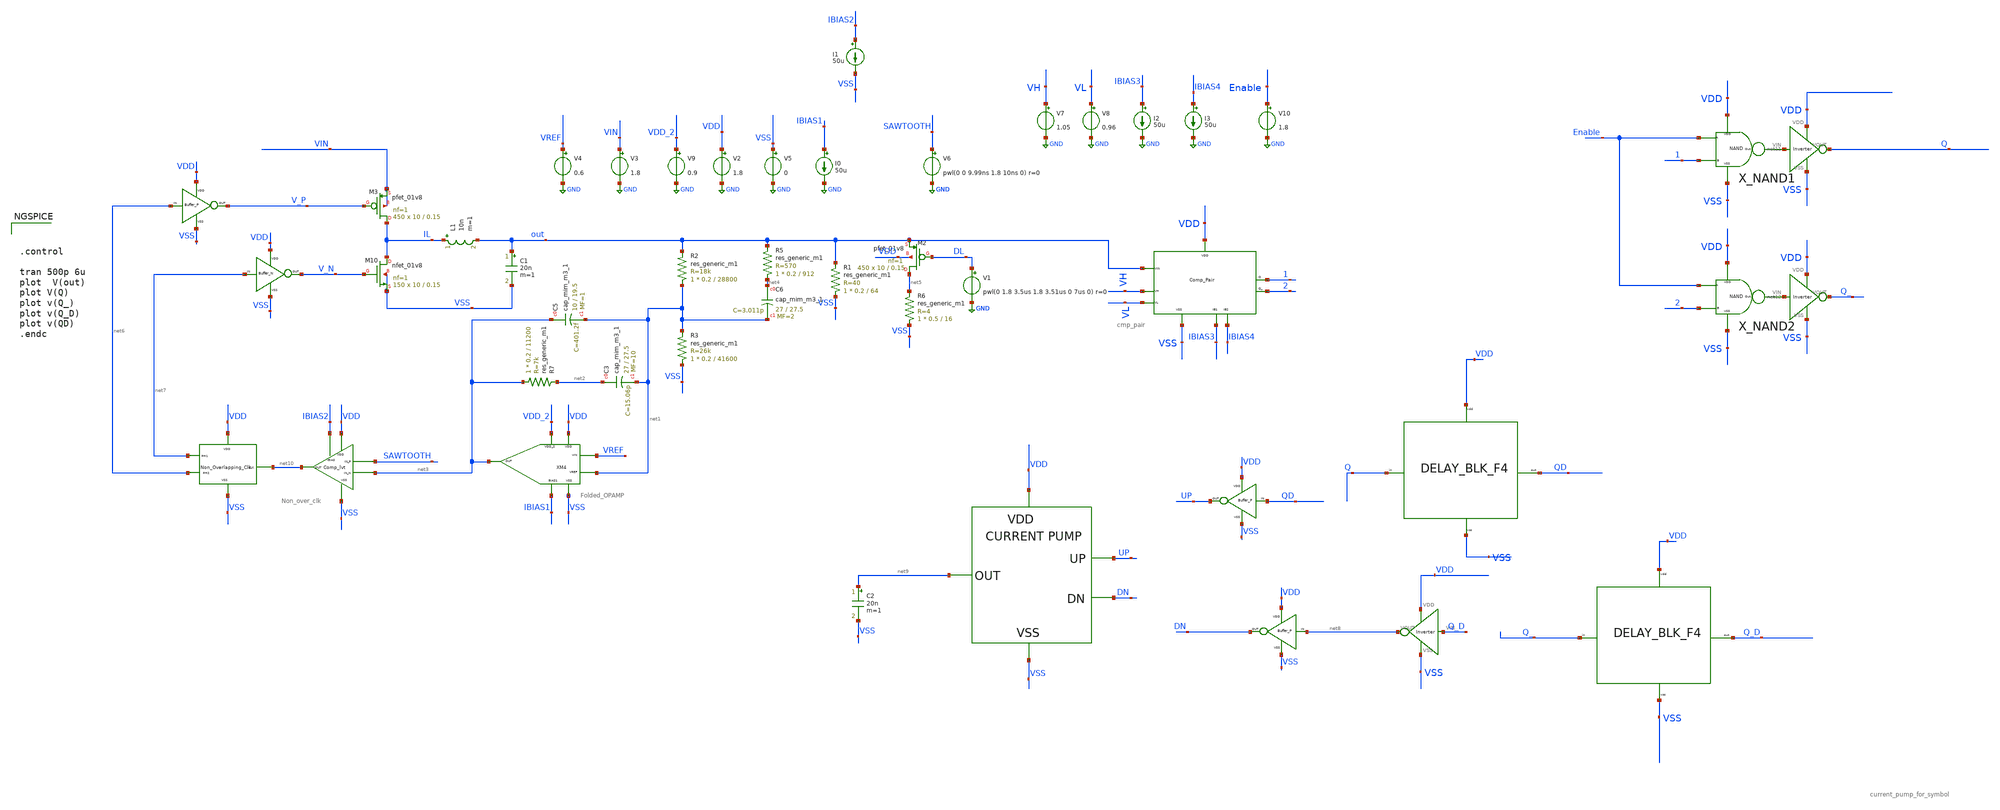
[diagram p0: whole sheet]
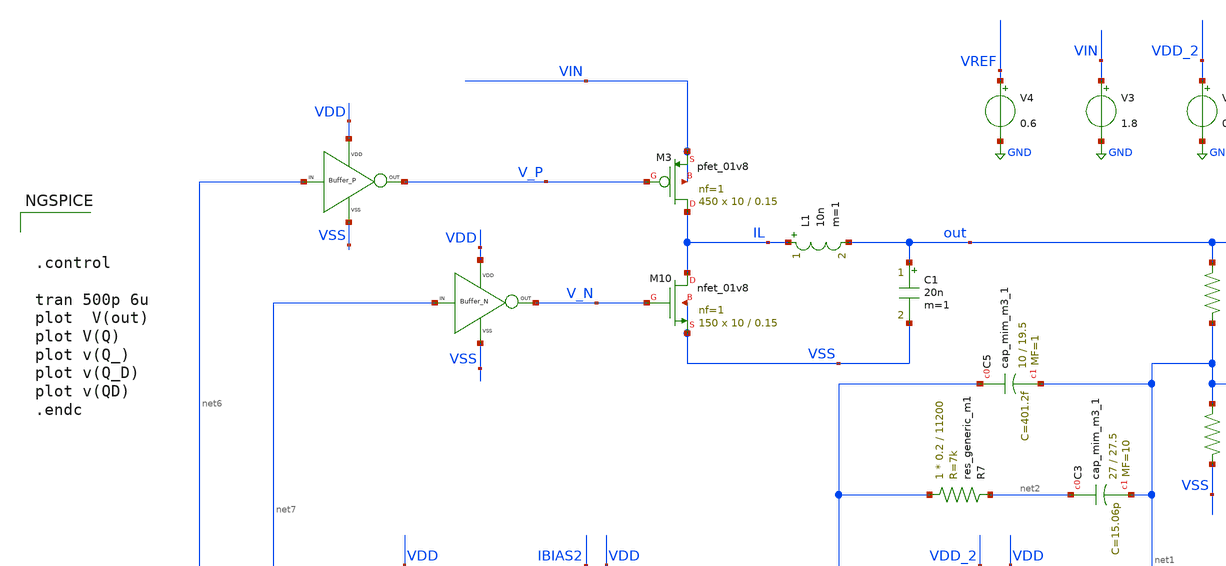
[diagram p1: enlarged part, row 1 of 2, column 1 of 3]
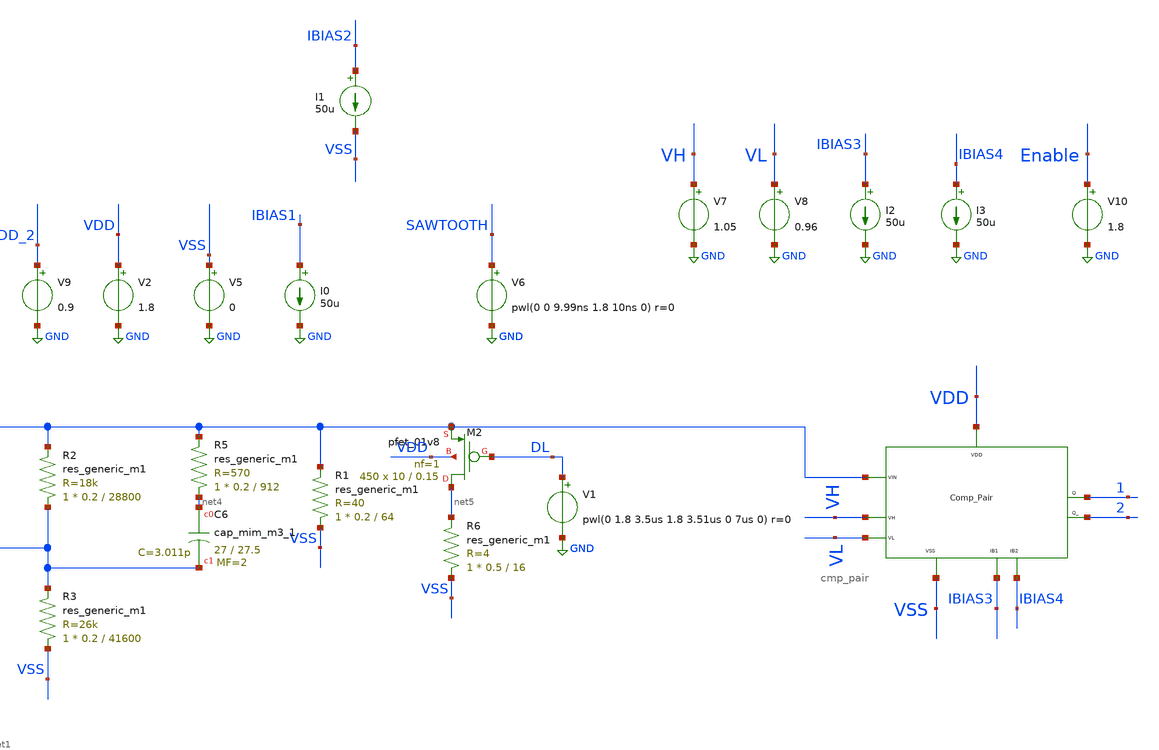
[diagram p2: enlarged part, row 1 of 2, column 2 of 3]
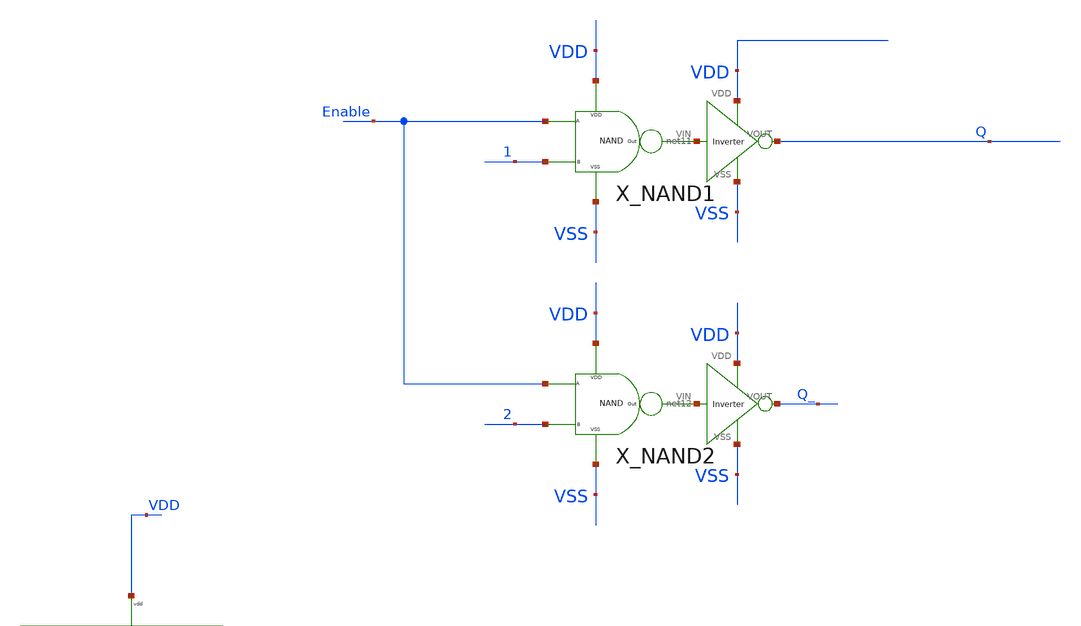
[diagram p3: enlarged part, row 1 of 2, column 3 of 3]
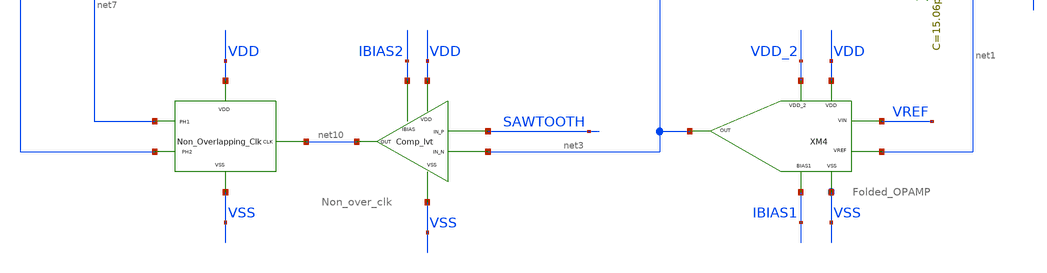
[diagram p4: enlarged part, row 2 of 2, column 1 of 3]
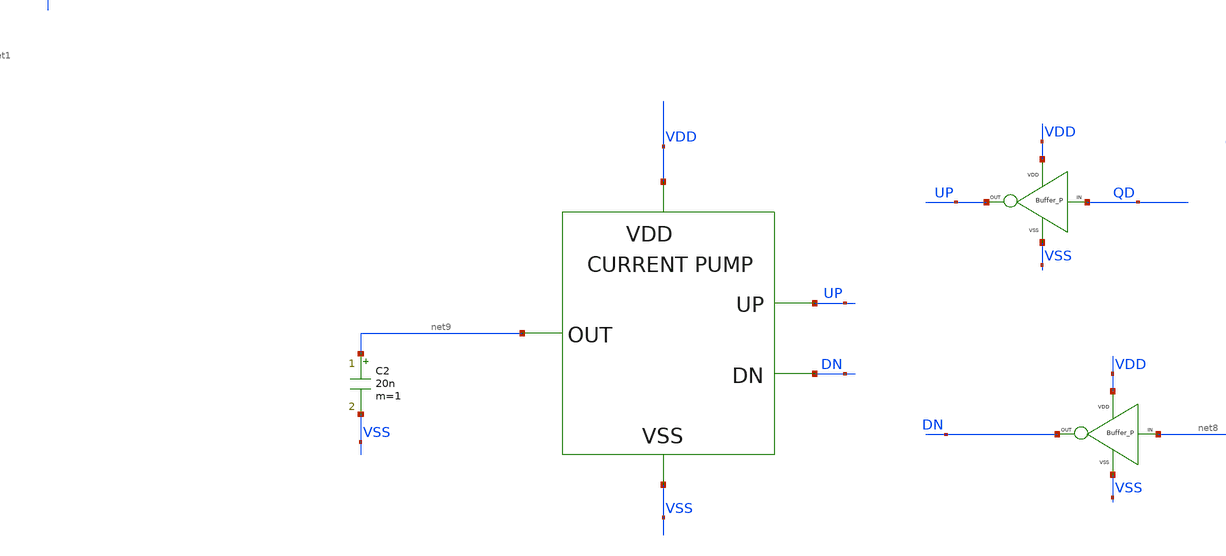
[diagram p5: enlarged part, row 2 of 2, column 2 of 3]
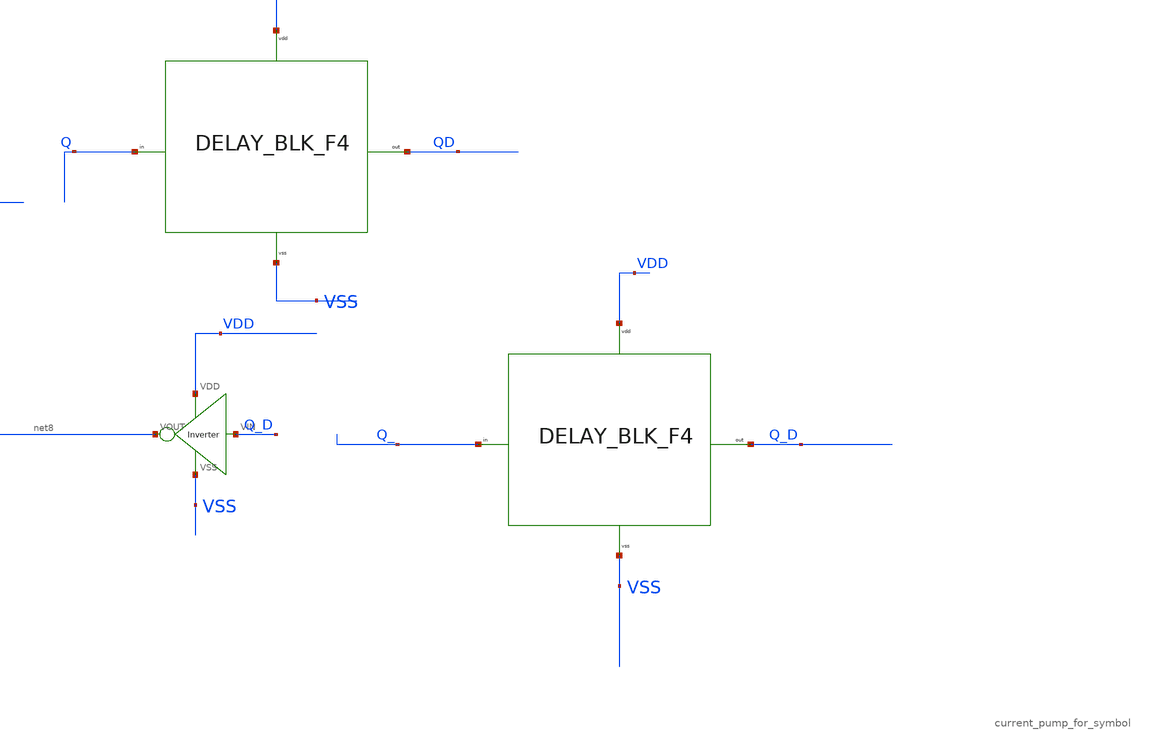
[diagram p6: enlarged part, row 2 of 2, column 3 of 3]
** sch_path: xschem/DC_DC_Converter_xschem/OTHERS/DC_DC_Converter_JV8/TOP_LEVEL/closed_loop_v10.sch
**.subckt closed_loop_v10
XM3 IL V_P VIN VIN sky130_fd_pr__pfet_01v8 L=0.15 W=10 nf=1 ad='int((nf+1)/2) * W/nf * 0.29' as='int((nf+2)/2) * W/nf * 0.29'
+ pd='2*int((nf+1)/2) * (W/nf + 0.29)' ps='2*int((nf+2)/2) * (W/nf + 0.29)' nrd='0.29 / W' nrs='0.29 / W'
+ sa=0 sb=0 sd=0 mult=450 m=450
L1 IL out 10n m=1
C1 out VSS 20n m=1
V3 VIN GND 1.8
I0 IBIAS1 GND 50u
V9 VDD_2 GND 0.9
V2 VDD GND 1.8
V5 VSS GND 0
V4 VREF GND 0.6
I1 IBIAS2 VSS 50u
V6 SAWTOOTH GND pwl(0 0 9.99ns 1.8 10ns 0) r=0
XM2 net5 DL out VDD sky130_fd_pr__pfet_01v8 L=0.15 W=10 nf=1 ad='int((nf+1)/2) * W/nf * 0.29' as='int((nf+2)/2) * W/nf * 0.29'
+ pd='2*int((nf+1)/2) * (W/nf + 0.29)' ps='2*int((nf+2)/2) * (W/nf + 0.29)' nrd='0.29 / W' nrs='0.29 / W'
+ sa=0 sb=0 sd=0 mult=450 m=450
V1 DL GND pwl(0 1.8 3.5us 1.8 3.51us 0 7us 0) r=0
X1 net6 V_P VDD VSS BUFFER_P
X2 net7 V_N VDD VSS BUFFER_N
XM3 net10 VDD VSS net7 net6 Non_over_clk
XM4 VDD VSS VDD_2 IBIAS1 net3 VREF net1 Folded_OPAMP
V7 VH GND 1.05
V8 VL GND 0.96
I2 IBIAS3 GND 50u
I3 IBIAS4 GND 50u
XM1 VDD VSS out VH VL IBIAS3 IBIAS4 1 2 cmp_pair
X5 net8 DN VDD VSS BUFFER_P
X6 QD UP VDD VSS BUFFER_P
X7 UP net9 VDD VSS DN current_pump_for_symbol
X_NAND1 VDD VSS Enable 1 net11 NAND
X_NAND2 VDD VSS Enable 2 net12 NAND
X9 VSS VDD net11 Q Inverter
X10 VSS VDD net12 Q_ Inverter
XC5 net3 net1 sky130_fd_pr__cap_mim_m3_1 W=10 L=19.5 MF=1 m=1
XC3 net2 net1 sky130_fd_pr__cap_mim_m3_1 W=27 L=27.5 MF=10 m=10
R7 net3 net2 sky130_fd_pr__res_generic_m1 W=0.2 L=11200 m=1
R6 VSS net5 sky130_fd_pr__res_generic_m1 W=0.5 L=16 m=1
R1 VSS out sky130_fd_pr__res_generic_m1 W=0.2 L=64 m=1
R5 net4 out sky130_fd_pr__res_generic_m1 W=0.2 L=912 m=1
R2 net1 out sky130_fd_pr__res_generic_m1 W=0.2 L=28800 m=1
R3 VSS net1 sky130_fd_pr__res_generic_m1 W=0.2 L=41600 m=1
V10 Enable GND 1.8
XC6 net4 net1 sky130_fd_pr__cap_mim_m3_1 W=27 L=27.5 MF=2 m=2
X3 VSS VDD Q_D net8 Inverter
XM10 IL V_N VSS VSS sky130_fd_pr__nfet_01v8 L=0.15 W=10 nf=1 ad='int((nf+1)/2) * W/nf * 0.29' as='int((nf+2)/2) * W/nf * 0.29'
+ pd='2*int((nf+1)/2) * (W/nf + 0.29)' ps='2*int((nf+2)/2) * (W/nf + 0.29)' nrd='0.29 / W' nrs='0.29 / W'
+ sa=0 sb=0 sd=0 mult=150 m=150
X4 Q QD VDD VSS Delay_BLK_F4
X8 Q_ Q_D VDD VSS Delay_BLK_F4
C2 net9 VSS 20n m=1
XM2 IBIAS2 VDD SAWTOOTH net3 VSS net10 Comp_lvt
**** begin user architecture code

** opencircuitdesign pdks install
.lib $::SKYWATER_MODELS/sky130.lib.spice tt





.control

tran 500p 6u
plot  V(out)
plot V(Q)
plot v(Q_)
plot v(Q_D)
plot v(QD)
.endc


**** end user architecture code
**.ends
.GLOBAL GND
.end
